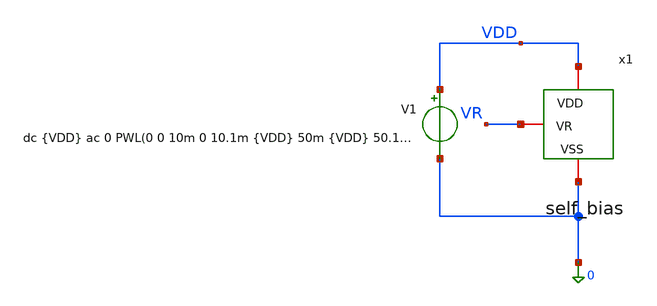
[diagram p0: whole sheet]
** sch_path: xschem/Iref/self_bias_tb.sch
**.subckt self_bias_tb
V1 VDD 0 dc {VDD} ac 0 PWL(0 0 10m 0 10.1m {VDD} 50m {VDD} 50.1m 0 100m 0 101m {VDD} 150m {VDD} 150.1m
+ 0 200m 0 300m {VDD} 400m {VDD} 400.1m 0)
x1 VDD VR 0 self_bias
**** begin user architecture code



**dc {VDD} ac 0 pulse(0 {VDD} 2u 10u 10u 40u 100u)
* 1. Inclusión de libreria de modelos Sky130 PRIMERO
.lib /foss/pdks/sky130A/libs.tech/ngspice/sky130.lib.spice ss_ll
.option temp=27
.option num_threads=8

**parametros_ldo
.param VDD = 1.98



.param tstart   = 10u
.param trise    = 200u
.param tfall    = 200u

.param tsim = 'tstart+2*trise+tfall'



.control
let tstart   = 10u
let trise    = 200u
let tfall    = 200u

let tsim = '$&tstart+4*$&trise+3*$&tfall'

save all



* Ms2 (pfet_01v8_lvt)
save @m.x1.xMs2.msky130_fd_pr__pfet_01v8_lvt[gm]
save @m.x1.xMs2.msky130_fd_pr__pfet_01v8_lvt[gds]
save @m.x1.xMs2.msky130_fd_pr__pfet_01v8_lvt[id]
save @m.x1.xMs2.msky130_fd_pr__pfet_01v8_lvt[vgs]
save @m.x1.xMs2.msky130_fd_pr__pfet_01v8_lvt[vds]
save @m.x1.xMs2.msky130_fd_pr__pfet_01v8_lvt[vth]
save @m.x1.xMs2.msky130_fd_pr__pfet_01v8_lvt[vdsat]

* Mp3 (pfet_01v8_lvt)
save @m.x1.xMp3.msky130_fd_pr__pfet_01v8_lvt[gm]
save @m.x1.xMp3.msky130_fd_pr__pfet_01v8_lvt[gds]
save @m.x1.xMp3.msky130_fd_pr__pfet_01v8_lvt[id]
save @m.x1.xMp3.msky130_fd_pr__pfet_01v8_lvt[vgs]
save @m.x1.xMp3.msky130_fd_pr__pfet_01v8_lvt[vds]
save @m.x1.xMp3.msky130_fd_pr__pfet_01v8_lvt[vth]
save @m.x1.xMp3.msky130_fd_pr__pfet_01v8_lvt[vdsat]

* Mp4 (pfet_01v8_lvt)
save @m.x1.xMp4.msky130_fd_pr__pfet_01v8_lvt[gm]
save @m.x1.xMp4.msky130_fd_pr__pfet_01v8_lvt[gds]
save @m.x1.xMp4.msky130_fd_pr__pfet_01v8_lvt[id]
save @m.x1.xMp4.msky130_fd_pr__pfet_01v8_lvt[vgs]
save @m.x1.xMp4.msky130_fd_pr__pfet_01v8_lvt[vds]
save @m.x1.xMp4.msky130_fd_pr__pfet_01v8_lvt[vth]
save @m.x1.xMp4.msky130_fd_pr__pfet_01v8_lvt[vdsat]



*Ms1 (nfet_01v8)
save @m.x1.xMs1.msky130_fd_pr__nfet_01v8[gm]
save @m.x1.xMs1.msky130_fd_pr__nfet_01v8[gds]
save @m.x1.xMs1.msky130_fd_pr__nfet_01v8[id]
save @m.x1.xMs1.msky130_fd_pr__nfet_01v8[vgs]
save @m.x1.xMs1.msky130_fd_pr__nfet_01v8[vds]
save @m.x1.xMs1.msky130_fd_pr__nfet_01v8[vth]
save @m.x1.xMs1.msky130_fd_pr__nfet_01v8[vdsat]

*Ms3 (nfet_01v8)
save @m.x1.xMs3.msky130_fd_pr__nfet_01v8[gm]
save @m.x1.xMs3.msky130_fd_pr__nfet_01v8[gds]
save @m.x1.xMs3.msky130_fd_pr__nfet_01v8[id]
save @m.x1.xMs3.msky130_fd_pr__nfet_01v8[vgs]
save @m.x1.xMs3.msky130_fd_pr__nfet_01v8[vds]
save @m.x1.xMs3.msky130_fd_pr__nfet_01v8[vth]
save @m.x1.xMs3.msky130_fd_pr__nfet_01v8[vdsat]

*Mn1 (nfet_01v8)
save @m.x1.xMn1.msky130_fd_pr__nfet_01v8[gm]
save @m.x1.xMn1.msky130_fd_pr__nfet_01v8[gds]
save @m.x1.xMn1.msky130_fd_pr__nfet_01v8[id]
save @m.x1.xMn1.msky130_fd_pr__nfet_01v8[vgs]
save @m.x1.xMn1.msky130_fd_pr__nfet_01v8[vds]
save @m.x1.xMn1.msky130_fd_pr__nfet_01v8[vth]
save @m.x1.xMn1.msky130_fd_pr__nfet_01v8[vdsat]

*Mn2 (nfet_01v8)
save @m.x1.xMn2.msky130_fd_pr__nfet_01v8[gm]
save @m.x1.xMn2.msky130_fd_pr__nfet_01v8[gds]
save @m.x1.xMn2.msky130_fd_pr__nfet_01v8[id]
save @m.x1.xMn2.msky130_fd_pr__nfet_01v8[vgs]
save @m.x1.xMn2.msky130_fd_pr__nfet_01v8[vds]
save @m.x1.xMn2.msky130_fd_pr__nfet_01v8[vth]
save @m.x1.xMn2.msky130_fd_pr__nfet_01v8[vdsat]



set filetype=ascii
op
write self_bias_tb.raw

* 1. Calculamos y guardamos los valores
let vr = v(vr)
let ibias_val_uA_op = '(@m.x1.xMp4.msky130_fd_pr__pfet_01v8_lvt[id])*1000000'


* 2. Imprimimos el texto junto con el valor de la variable
echo VR = $&vr
echo ibias = $&ibias_val_uA_op

tran 2u 400.1m

* --- 3. Mediciones del Start-up ---
  * Midiendo voltaje vr justo antes de que el pulso respectivo se apague

  * Para Trise = 100us (Pulso activo entre 10m y 50m)
  meas tran vr_100us FIND v(vr) at=40m

  * Para Trise = 1ms (Pulso activo entre 100m y 150m)
  meas tran vr_1ms FIND v(vr) at=140m

  * Para Trise = 100ms (Pulso activo entre 200m y 400m)
  meas tran vr_100ms FIND v(vr) at=390m


.endc



**** end user architecture code
**.ends

* expanding   symbol:  self_bias.sym # of pins=3
** sym_path: xschem/Iref/self_bias.sym
** sch_path: xschem/Iref/self_bias.sch
.subckt self_bias VDD VR VSS
*.iopin VR
*.iopin VDD
*.iopin VSS
XMp4 vgp_self vgp_self VDD VDD sky130_fd_pr__pfet_01v8_lvt L=1 W=30 nf=6 ad='int((6 + 1)/2) * 30 / 6 * 0.29'
+ as='int((6 + 2)/2) * 30 / 6 * 0.29' pd='2*int((6 + 1)/2) * (30 / 6 + 0.29)' ps='2*int((6 + 2)/2) * (30 / 6 + 0.29)'
+ nrd='0.29 / 30 ' nrs='0.29 / 30 ' sa=0 sb=0 sd=0 mult=1 m=1
XMp3 VDI vgp_self VDD VDD sky130_fd_pr__pfet_01v8_lvt L=1 W=30 nf=6 ad='int((6 + 1)/2) * 30 / 6 * 0.29'
+ as='int((6 + 2)/2) * 30 / 6 * 0.29' pd='2*int((6 + 1)/2) * (30 / 6 + 0.29)' ps='2*int((6 + 2)/2) * (30 / 6 + 0.29)'
+ nrd='0.29 / 30 ' nrs='0.29 / 30 ' sa=0 sb=0 sd=0 mult=1 m=1
XMs2 VDinv VR vp1 VDD sky130_fd_pr__pfet_01v8_lvt L=5 W=0.5 nf=1 ad='int((1 + 1)/2) * 0.5 / 1 * 0.29'
+ as='int((1 + 2)/2) * 0.5 / 1 * 0.29' pd='2*int((1 + 1)/2) * (0.5 / 1 + 0.29)' ps='2*int((1 + 2)/2) * (0.5 / 1 + 0.29)'
+ nrd='0.29 / 0.5 ' nrs='0.29 / 0.5 ' sa=0 sb=0 sd=0 mult=1 m=1
XMn2 vgp_self VDI VR VSS sky130_fd_pr__nfet_01v8 L=1 W=24 nf=6 ad='int((6 + 1)/2) * 24 / 6 * 0.29' as='int((6 + 2)/2) * 24 / 6 * 0.29'
+ pd='2*int((6 + 1)/2) * (24 / 6 + 0.29)' ps='2*int((6 + 2)/2) * (24 / 6 + 0.29)' nrd='0.29 / 24 ' nrs='0.29 / 24 '
+ sa=0 sb=0 sd=0 mult=1 m=1
XMn1 VDI VR VSS VSS sky130_fd_pr__nfet_01v8 L=1 W=5 nf=5 ad='int((5 + 1)/2) * 5 / 5 * 0.29' as='int((5 + 2)/2) * 5 / 5 * 0.29'
+ pd='2*int((5 + 1)/2) * (5 / 5 + 0.29)' ps='2*int((5 + 2)/2) * (5 / 5 + 0.29)' nrd='0.29 / 5 ' nrs='0.29 / 5 '
+ sa=0 sb=0 sd=0 mult=1 m=1
XMs3 VDinv VR VSS VSS sky130_fd_pr__nfet_01v8 L=1 W=20 nf=5 ad='int((5 + 1)/2) * 20 / 5 * 0.29' as='int((5 + 2)/2) * 20 / 5 * 0.29'
+ pd='2*int((5 + 1)/2) * (20 / 5 + 0.29)' ps='2*int((5 + 2)/2) * (20 / 5 + 0.29)' nrd='0.29 / 20 ' nrs='0.29 / 20 '
+ sa=0 sb=0 sd=0 mult=1 m=1
XMs1 vgp_self VDinv VSS VSS sky130_fd_pr__nfet_01v8 L=1 W=2 nf=2 ad='int((2 + 1)/2) * 2 / 2 * 0.29' as='int((2 + 2)/2) * 2 / 2 * 0.29'
+ pd='2*int((2 + 1)/2) * (2 / 2 + 0.29)' ps='2*int((2 + 2)/2) * (2 / 2 + 0.29)' nrd='0.29 / 2 ' nrs='0.29 / 2 '
+ sa=0 sb=0 sd=0 mult=1 m=1
XR11 VSS VR VSS sky130_fd_pr__res_xhigh_po_0p69 L=20.7 mult=1 m=1
XMs4 vp1 VR vp2 VDD sky130_fd_pr__pfet_01v8_lvt L=5 W=0.5 nf=1 ad='int((1 + 1)/2) * 0.5 / 1 * 0.29' as='int((1 + 2)/2) * 0.5 / 1 * 0.29'
+ pd='2*int((1 + 1)/2) * (0.5 / 1 + 0.29)' ps='2*int((1 + 2)/2) * (0.5 / 1 + 0.29)' nrd='0.29 / 0.5 ' nrs='0.29 / 0.5 '
+ sa=0 sb=0 sd=0 mult=1 m=1
XMs5 vp2 VR vp3 VDD sky130_fd_pr__pfet_01v8_lvt L=5 W=0.5 nf=1 ad='int((1 + 1)/2) * 0.5 / 1 * 0.29' as='int((1 + 2)/2) * 0.5 / 1 * 0.29'
+ pd='2*int((1 + 1)/2) * (0.5 / 1 + 0.29)' ps='2*int((1 + 2)/2) * (0.5 / 1 + 0.29)' nrd='0.29 / 0.5 ' nrs='0.29 / 0.5 '
+ sa=0 sb=0 sd=0 mult=1 m=1
XMs6 vp3 VR vp4 VDD sky130_fd_pr__pfet_01v8_lvt L=5 W=0.5 nf=1 ad='int((1 + 1)/2) * 0.5 / 1 * 0.29' as='int((1 + 2)/2) * 0.5 / 1 * 0.29'
+ pd='2*int((1 + 1)/2) * (0.5 / 1 + 0.29)' ps='2*int((1 + 2)/2) * (0.5 / 1 + 0.29)' nrd='0.29 / 0.5 ' nrs='0.29 / 0.5 '
+ sa=0 sb=0 sd=0 mult=1 m=1
XMs7 vp4 VR VDD VDD sky130_fd_pr__pfet_01v8_lvt L=5 W=0.5 nf=1 ad='int((1 + 1)/2) * 0.5 / 1 * 0.29' as='int((1 + 2)/2) * 0.5 / 1 * 0.29'
+ pd='2*int((1 + 1)/2) * (0.5 / 1 + 0.29)' ps='2*int((1 + 2)/2) * (0.5 / 1 + 0.29)' nrd='0.29 / 0.5 ' nrs='0.29 / 0.5 '
+ sa=0 sb=0 sd=0 mult=1 m=1
.ends

.end
